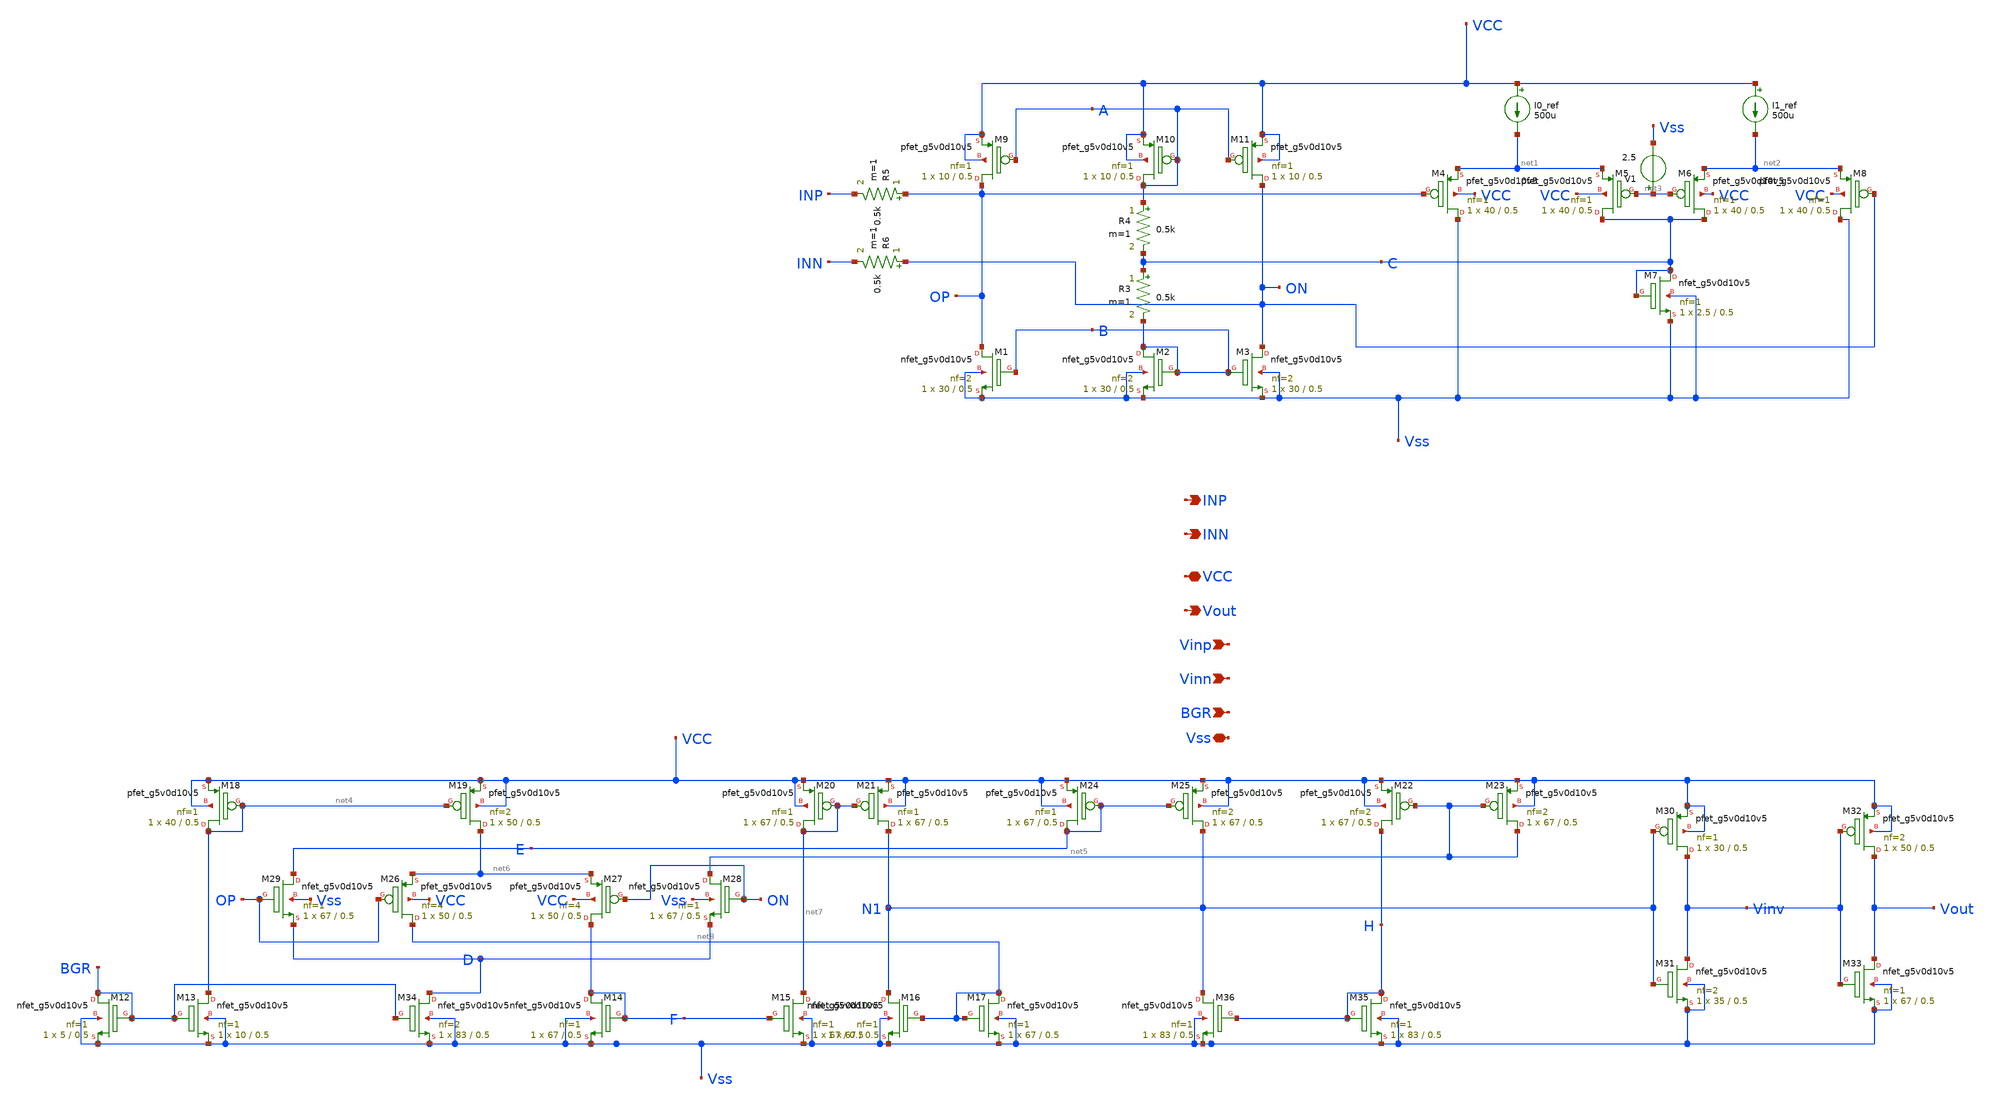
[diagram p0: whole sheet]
** sch_path: Git Files/Schematic/Reciever_Netlist.sch
**.subckt Reciever_Netlist Vinp Vinn Vout VCC INN INP BGR Vss
*.ipin Vinp
*.ipin Vinn
*.opin Vout
*.iopin VCC
*.opin INN
*.opin INP
*.ipin BGR
*.iopin Vss
XM1 OP B Vss Vss sky130_fd_pr__nfet_g5v0d10v5 L=0.5 W=30 nf=2 ad='int((nf+1)/2) * W/nf * 0.29' as='int((nf+2)/2) * W/nf * 0.29'
+ pd='2*int((nf+1)/2) * (W/nf + 0.29)' ps='2*int((nf+2)/2) * (W/nf + 0.29)' nrd='0.29 / W' nrs='0.29 / W'
+ sa=0 sb=0 sd=0 mult=1 m=1
XM2 B B Vss Vss sky130_fd_pr__nfet_g5v0d10v5 L=0.5 W=30 nf=2 ad='int((nf+1)/2) * W/nf * 0.29' as='int((nf+2)/2) * W/nf * 0.29'
+ pd='2*int((nf+1)/2) * (W/nf + 0.29)' ps='2*int((nf+2)/2) * (W/nf + 0.29)' nrd='0.29 / W' nrs='0.29 / W'
+ sa=0 sb=0 sd=0 mult=1 m=1
XM3 ON B Vss Vss sky130_fd_pr__nfet_g5v0d10v5 L=0.5 W=30 nf=2 ad='int((nf+1)/2) * W/nf * 0.29' as='int((nf+2)/2) * W/nf * 0.29'
+ pd='2*int((nf+1)/2) * (W/nf + 0.29)' ps='2*int((nf+2)/2) * (W/nf + 0.29)' nrd='0.29 / W' nrs='0.29 / W'
+ sa=0 sb=0 sd=0 mult=1 m=1
XM9 OP A VCC VCC sky130_fd_pr__pfet_g5v0d10v5 L=0.5 W=10 nf=1 ad='int((nf+1)/2) * W/nf * 0.29' as='int((nf+2)/2) * W/nf * 0.29'
+ pd='2*int((nf+1)/2) * (W/nf + 0.29)' ps='2*int((nf+2)/2) * (W/nf + 0.29)' nrd='0.29 / W' nrs='0.29 / W'
+ sa=0 sb=0 sd=0 mult=1 m=1
XM10 A A VCC VCC sky130_fd_pr__pfet_g5v0d10v5 L=0.5 W=10 nf=1 ad='int((nf+1)/2) * W/nf * 0.29' as='int((nf+2)/2) * W/nf * 0.29'
+ pd='2*int((nf+1)/2) * (W/nf + 0.29)' ps='2*int((nf+2)/2) * (W/nf + 0.29)' nrd='0.29 / W' nrs='0.29 / W'
+ sa=0 sb=0 sd=0 mult=1 m=1
XM11 ON A VCC VCC sky130_fd_pr__pfet_g5v0d10v5 L=0.5 W=10 nf=1 ad='int((nf+1)/2) * W/nf * 0.29' as='int((nf+2)/2) * W/nf * 0.29'
+ pd='2*int((nf+1)/2) * (W/nf + 0.29)' ps='2*int((nf+2)/2) * (W/nf + 0.29)' nrd='0.29 / W' nrs='0.29 / W'
+ sa=0 sb=0 sd=0 mult=1 m=1
I0_ref VCC net1 500u
I1_ref VCC net2 500u
R3 C B 0.5k m=1
R4 A C 0.5k m=1
R5 OP INP 0.5k m=1
R6 ON INN 0.5k m=1
XM7 C C Vss Vss sky130_fd_pr__nfet_g5v0d10v5 L=0.5 W=2.5 nf=1 ad='int((nf+1)/2) * W/nf * 0.29' as='int((nf+2)/2) * W/nf * 0.29'
+ pd='2*int((nf+1)/2) * (W/nf + 0.29)' ps='2*int((nf+2)/2) * (W/nf + 0.29)' nrd='0.29 / W' nrs='0.29 / W'
+ sa=0 sb=0 sd=0 mult=1 m=1
XM4 Vss OP net1 VCC sky130_fd_pr__pfet_g5v0d10v5 L=0.5 W=40 nf=1 ad='int((nf+1)/2) * W/nf * 0.29' as='int((nf+2)/2) * W/nf * 0.29'
+ pd='2*int((nf+1)/2) * (W/nf + 0.29)' ps='2*int((nf+2)/2) * (W/nf + 0.29)' nrd='0.29 / W' nrs='0.29 / W'
+ sa=0 sb=0 sd=0 mult=1 m=1
XM5 C net3 net1 VCC sky130_fd_pr__pfet_g5v0d10v5 L=0.5 W=40 nf=1 ad='int((nf+1)/2) * W/nf * 0.29' as='int((nf+2)/2) * W/nf * 0.29'
+ pd='2*int((nf+1)/2) * (W/nf + 0.29)' ps='2*int((nf+2)/2) * (W/nf + 0.29)' nrd='0.29 / W' nrs='0.29 / W'
+ sa=0 sb=0 sd=0 mult=1 m=1
XM6 C net3 net2 VCC sky130_fd_pr__pfet_g5v0d10v5 L=0.5 W=40 nf=1 ad='int((nf+1)/2) * W/nf * 0.29' as='int((nf+2)/2) * W/nf * 0.29'
+ pd='2*int((nf+1)/2) * (W/nf + 0.29)' ps='2*int((nf+2)/2) * (W/nf + 0.29)' nrd='0.29 / W' nrs='0.29 / W'
+ sa=0 sb=0 sd=0 mult=1 m=1
XM8 Vss ON net2 VCC sky130_fd_pr__pfet_g5v0d10v5 L=0.5 W=40 nf=1 ad='int((nf+1)/2) * W/nf * 0.29' as='int((nf+2)/2) * W/nf * 0.29'
+ pd='2*int((nf+1)/2) * (W/nf + 0.29)' ps='2*int((nf+2)/2) * (W/nf + 0.29)' nrd='0.29 / W' nrs='0.29 / W'
+ sa=0 sb=0 sd=0 mult=1 m=1
V1 net3 Vss 2.5
XM12 BGR BGR Vss Vss sky130_fd_pr__nfet_g5v0d10v5 L=0.5 W=5 nf=1 ad='int((nf+1)/2) * W/nf * 0.29' as='int((nf+2)/2) * W/nf * 0.29'
+ pd='2*int((nf+1)/2) * (W/nf + 0.29)' ps='2*int((nf+2)/2) * (W/nf + 0.29)' nrd='0.29 / W' nrs='0.29 / W'
+ sa=0 sb=0 sd=0 mult=1 m=1
XM13 net4 BGR Vss Vss sky130_fd_pr__nfet_g5v0d10v5 L=0.5 W=10 nf=1 ad='int((nf+1)/2) * W/nf * 0.29' as='int((nf+2)/2) * W/nf * 0.29'
+ pd='2*int((nf+1)/2) * (W/nf + 0.29)' ps='2*int((nf+2)/2) * (W/nf + 0.29)' nrd='0.29 / W' nrs='0.29 / W'
+ sa=0 sb=0 sd=0 mult=1 m=1
XM14 F F Vss Vss sky130_fd_pr__nfet_g5v0d10v5 L=0.5 W=67 nf=1 ad='int((nf+1)/2) * W/nf * 0.29' as='int((nf+2)/2) * W/nf * 0.29'
+ pd='2*int((nf+1)/2) * (W/nf + 0.29)' ps='2*int((nf+2)/2) * (W/nf + 0.29)' nrd='0.29 / W' nrs='0.29 / W'
+ sa=0 sb=0 sd=0 mult=1 m=1
XM15 net7 F Vss Vss sky130_fd_pr__nfet_g5v0d10v5 L=0.5 W=67 nf=1 ad='int((nf+1)/2) * W/nf * 0.29' as='int((nf+2)/2) * W/nf * 0.29'
+ pd='2*int((nf+1)/2) * (W/nf + 0.29)' ps='2*int((nf+2)/2) * (W/nf + 0.29)' nrd='0.29 / W' nrs='0.29 / W'
+ sa=0 sb=0 sd=0 mult=1 m=1
XM16 N1 net8 Vss Vss sky130_fd_pr__nfet_g5v0d10v5 L=0.5 W=67 nf=1 ad='int((nf+1)/2) * W/nf * 0.29' as='int((nf+2)/2) * W/nf * 0.29'
+ pd='2*int((nf+1)/2) * (W/nf + 0.29)' ps='2*int((nf+2)/2) * (W/nf + 0.29)' nrd='0.29 / W' nrs='0.29 / W'
+ sa=0 sb=0 sd=0 mult=1 m=1
XM17 net8 net8 Vss Vss sky130_fd_pr__nfet_g5v0d10v5 L=0.5 W=67 nf=1 ad='int((nf+1)/2) * W/nf * 0.29'
+ as='int((nf+2)/2) * W/nf * 0.29' pd='2*int((nf+1)/2) * (W/nf + 0.29)' ps='2*int((nf+2)/2) * (W/nf + 0.29)'
+ nrd='0.29 / W' nrs='0.29 / W' sa=0 sb=0 sd=0 mult=1 m=1
XM18 net4 net4 VCC VCC sky130_fd_pr__pfet_g5v0d10v5 L=0.5 W=40 nf=1 ad='int((nf+1)/2) * W/nf * 0.29'
+ as='int((nf+2)/2) * W/nf * 0.29' pd='2*int((nf+1)/2) * (W/nf + 0.29)' ps='2*int((nf+2)/2) * (W/nf + 0.29)'
+ nrd='0.29 / W' nrs='0.29 / W' sa=0 sb=0 sd=0 mult=1 m=1
XM19 net6 net4 VCC VCC sky130_fd_pr__pfet_g5v0d10v5 L=0.5 W=50 nf=2 ad='int((nf+1)/2) * W/nf * 0.29'
+ as='int((nf+2)/2) * W/nf * 0.29' pd='2*int((nf+1)/2) * (W/nf + 0.29)' ps='2*int((nf+2)/2) * (W/nf + 0.29)'
+ nrd='0.29 / W' nrs='0.29 / W' sa=0 sb=0 sd=0 mult=1 m=1
XM20 net7 net7 VCC VCC sky130_fd_pr__pfet_g5v0d10v5 L=0.5 W=67 nf=1 ad='int((nf+1)/2) * W/nf * 0.29'
+ as='int((nf+2)/2) * W/nf * 0.29' pd='2*int((nf+1)/2) * (W/nf + 0.29)' ps='2*int((nf+2)/2) * (W/nf + 0.29)'
+ nrd='0.29 / W' nrs='0.29 / W' sa=0 sb=0 sd=0 mult=1 m=1
XM21 N1 net7 VCC VCC sky130_fd_pr__pfet_g5v0d10v5 L=0.5 W=67 nf=1 ad='int((nf+1)/2) * W/nf * 0.29' as='int((nf+2)/2) * W/nf * 0.29'
+ pd='2*int((nf+1)/2) * (W/nf + 0.29)' ps='2*int((nf+2)/2) * (W/nf + 0.29)' nrd='0.29 / W' nrs='0.29 / W'
+ sa=0 sb=0 sd=0 mult=1 m=1
XM22 H net5 VCC VCC sky130_fd_pr__pfet_g5v0d10v5 L=0.5 W=67 nf=2 ad='int((nf+1)/2) * W/nf * 0.29' as='int((nf+2)/2) * W/nf * 0.29'
+ pd='2*int((nf+1)/2) * (W/nf + 0.29)' ps='2*int((nf+2)/2) * (W/nf + 0.29)' nrd='0.29 / W' nrs='0.29 / W'
+ sa=0 sb=0 sd=0 mult=1 m=1
XM23 net5 net5 VCC VCC sky130_fd_pr__pfet_g5v0d10v5 L=0.5 W=67 nf=2 ad='int((nf+1)/2) * W/nf * 0.29'
+ as='int((nf+2)/2) * W/nf * 0.29' pd='2*int((nf+1)/2) * (W/nf + 0.29)' ps='2*int((nf+2)/2) * (W/nf + 0.29)'
+ nrd='0.29 / W' nrs='0.29 / W' sa=0 sb=0 sd=0 mult=1 m=1
XM24 E E VCC VCC sky130_fd_pr__pfet_g5v0d10v5 L=0.5 W=67 nf=1 ad='int((nf+1)/2) * W/nf * 0.29' as='int((nf+2)/2) * W/nf * 0.29'
+ pd='2*int((nf+1)/2) * (W/nf + 0.29)' ps='2*int((nf+2)/2) * (W/nf + 0.29)' nrd='0.29 / W' nrs='0.29 / W'
+ sa=0 sb=0 sd=0 mult=1 m=1
XM25 N1 E VCC VCC sky130_fd_pr__pfet_g5v0d10v5 L=0.5 W=67 nf=2 ad='int((nf+1)/2) * W/nf * 0.29' as='int((nf+2)/2) * W/nf * 0.29'
+ pd='2*int((nf+1)/2) * (W/nf + 0.29)' ps='2*int((nf+2)/2) * (W/nf + 0.29)' nrd='0.29 / W' nrs='0.29 / W'
+ sa=0 sb=0 sd=0 mult=1 m=1
XM26 net8 OP net6 VCC sky130_fd_pr__pfet_g5v0d10v5 L=0.5 W=50 nf=4 ad='int((nf+1)/2) * W/nf * 0.29' as='int((nf+2)/2) * W/nf * 0.29'
+ pd='2*int((nf+1)/2) * (W/nf + 0.29)' ps='2*int((nf+2)/2) * (W/nf + 0.29)' nrd='0.29 / W' nrs='0.29 / W'
+ sa=0 sb=0 sd=0 mult=1 m=1
XM27 F ON net6 VCC sky130_fd_pr__pfet_g5v0d10v5 L=0.5 W=50 nf=4 ad='int((nf+1)/2) * W/nf * 0.29' as='int((nf+2)/2) * W/nf * 0.29'
+ pd='2*int((nf+1)/2) * (W/nf + 0.29)' ps='2*int((nf+2)/2) * (W/nf + 0.29)' nrd='0.29 / W' nrs='0.29 / W'
+ sa=0 sb=0 sd=0 mult=1 m=1
XM28 net5 ON D Vss sky130_fd_pr__nfet_g5v0d10v5 L=0.5 W=67 nf=1 ad='int((nf+1)/2) * W/nf * 0.29' as='int((nf+2)/2) * W/nf * 0.29'
+ pd='2*int((nf+1)/2) * (W/nf + 0.29)' ps='2*int((nf+2)/2) * (W/nf + 0.29)' nrd='0.29 / W' nrs='0.29 / W'
+ sa=0 sb=0 sd=0 mult=1 m=1
XM29 E OP D Vss sky130_fd_pr__nfet_g5v0d10v5 L=0.5 W=67 nf=1 ad='int((nf+1)/2) * W/nf * 0.29' as='int((nf+2)/2) * W/nf * 0.29'
+ pd='2*int((nf+1)/2) * (W/nf + 0.29)' ps='2*int((nf+2)/2) * (W/nf + 0.29)' nrd='0.29 / W' nrs='0.29 / W'
+ sa=0 sb=0 sd=0 mult=1 m=1
XM30 Vinv N1 VCC VCC sky130_fd_pr__pfet_g5v0d10v5 L=0.5 W=30 nf=1 ad='int((nf+1)/2) * W/nf * 0.29' as='int((nf+2)/2) * W/nf * 0.29'
+ pd='2*int((nf+1)/2) * (W/nf + 0.29)' ps='2*int((nf+2)/2) * (W/nf + 0.29)' nrd='0.29 / W' nrs='0.29 / W'
+ sa=0 sb=0 sd=0 mult=1 m=1
XM31 Vinv N1 Vss Vss sky130_fd_pr__nfet_g5v0d10v5 L=0.5 W=35 nf=2 ad='int((nf+1)/2) * W/nf * 0.29' as='int((nf+2)/2) * W/nf * 0.29'
+ pd='2*int((nf+1)/2) * (W/nf + 0.29)' ps='2*int((nf+2)/2) * (W/nf + 0.29)' nrd='0.29 / W' nrs='0.29 / W'
+ sa=0 sb=0 sd=0 mult=1 m=1
XM32 Vout Vinv VCC VCC sky130_fd_pr__pfet_g5v0d10v5 L=0.5 W=50 nf=2 ad='int((nf+1)/2) * W/nf * 0.29'
+ as='int((nf+2)/2) * W/nf * 0.29' pd='2*int((nf+1)/2) * (W/nf + 0.29)' ps='2*int((nf+2)/2) * (W/nf + 0.29)'
+ nrd='0.29 / W' nrs='0.29 / W' sa=0 sb=0 sd=0 mult=1 m=1
XM33 Vout Vinv Vss Vss sky130_fd_pr__nfet_g5v0d10v5 L=0.5 W=67 nf=1 ad='int((nf+1)/2) * W/nf * 0.29'
+ as='int((nf+2)/2) * W/nf * 0.29' pd='2*int((nf+1)/2) * (W/nf + 0.29)' ps='2*int((nf+2)/2) * (W/nf + 0.29)'
+ nrd='0.29 / W' nrs='0.29 / W' sa=0 sb=0 sd=0 mult=1 m=1
XM34 D BGR Vss Vss sky130_fd_pr__nfet_g5v0d10v5 L=0.5 W=83 nf=2 ad='int((nf+1)/2) * W/nf * 0.29' as='int((nf+2)/2) * W/nf * 0.29'
+ pd='2*int((nf+1)/2) * (W/nf + 0.29)' ps='2*int((nf+2)/2) * (W/nf + 0.29)' nrd='0.29 / W' nrs='0.29 / W'
+ sa=0 sb=0 sd=0 mult=1 m=1
XM35 H H Vss Vss sky130_fd_pr__nfet_g5v0d10v5 L=0.5 W=83 nf=1 ad='int((nf+1)/2) * W/nf * 0.29' as='int((nf+2)/2) * W/nf * 0.29'
+ pd='2*int((nf+1)/2) * (W/nf + 0.29)' ps='2*int((nf+2)/2) * (W/nf + 0.29)' nrd='0.29 / W' nrs='0.29 / W'
+ sa=0 sb=0 sd=0 mult=1 m=1
XM36 N1 H Vss Vss sky130_fd_pr__nfet_g5v0d10v5 L=0.5 W=83 nf=1 ad='int((nf+1)/2) * W/nf * 0.29' as='int((nf+2)/2) * W/nf * 0.29'
+ pd='2*int((nf+1)/2) * (W/nf + 0.29)' ps='2*int((nf+2)/2) * (W/nf + 0.29)' nrd='0.29 / W' nrs='0.29 / W'
+ sa=0 sb=0 sd=0 mult=1 m=1
**.ends
.end
